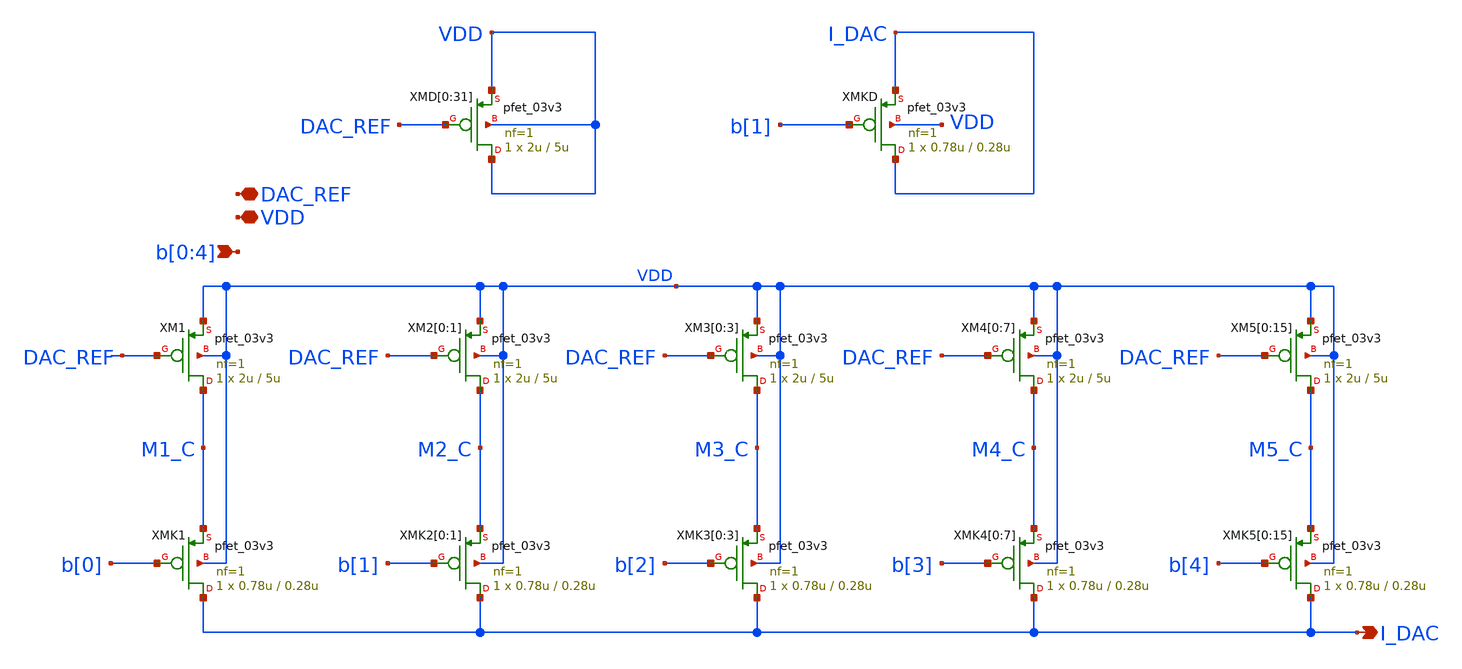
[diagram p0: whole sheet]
** sch_path: DAC_CORE_5bit/DAC_CORE_5bit.sch
**.subckt DAC_CORE_5bit I_DAC VDD DAC_REF b[0],b[1],b[2],b[3],b[4]
*.opin I_DAC
*.iopin VDD
*.iopin DAC_REF
*.ipin b[0],b[1],b[2],b[3],b[4]
XMK1 I_DAC b[0] M1_C VDD pfet_03v3 L=0.28u W=0.78u nf=1 ad='int((nf+1)/2) * W/nf * 0.18u' as='int((nf+2)/2) * W/nf * 0.18u'
+ pd='2*int((nf+1)/2) * (W/nf + 0.18u)' ps='2*int((nf+2)/2) * (W/nf + 0.18u)' nrd='0.18u / W' nrs='0.18u / W'
+ sa=0 sb=0 sd=0 m=1
XMK2[0] I_DAC b[1] M2_C VDD pfet_03v3 L=0.28u W=0.78u nf=1 ad='int((nf+1)/2) * W/nf * 0.18u' as='int((nf+2)/2) * W/nf * 0.18u'
+ pd='2*int((nf+1)/2) * (W/nf + 0.18u)' ps='2*int((nf+2)/2) * (W/nf + 0.18u)' nrd='0.18u / W' nrs='0.18u / W'
+ sa=0 sb=0 sd=0 m=1
XMK2[1] I_DAC b[1] M2_C VDD pfet_03v3 L=0.28u W=0.78u nf=1 ad='int((nf+1)/2) * W/nf * 0.18u' as='int((nf+2)/2) * W/nf * 0.18u'
+ pd='2*int((nf+1)/2) * (W/nf + 0.18u)' ps='2*int((nf+2)/2) * (W/nf + 0.18u)' nrd='0.18u / W' nrs='0.18u / W'
+ sa=0 sb=0 sd=0 m=1
XMK3[0] I_DAC b[2] M3_C VDD pfet_03v3 L=0.28u W=0.78u nf=1 ad='int((nf+1)/2) * W/nf * 0.18u' as='int((nf+2)/2) * W/nf * 0.18u'
+ pd='2*int((nf+1)/2) * (W/nf + 0.18u)' ps='2*int((nf+2)/2) * (W/nf + 0.18u)' nrd='0.18u / W' nrs='0.18u / W'
+ sa=0 sb=0 sd=0 m=1
XMK3[1] I_DAC b[2] M3_C VDD pfet_03v3 L=0.28u W=0.78u nf=1 ad='int((nf+1)/2) * W/nf * 0.18u' as='int((nf+2)/2) * W/nf * 0.18u'
+ pd='2*int((nf+1)/2) * (W/nf + 0.18u)' ps='2*int((nf+2)/2) * (W/nf + 0.18u)' nrd='0.18u / W' nrs='0.18u / W'
+ sa=0 sb=0 sd=0 m=1
XMK3[2] I_DAC b[2] M3_C VDD pfet_03v3 L=0.28u W=0.78u nf=1 ad='int((nf+1)/2) * W/nf * 0.18u' as='int((nf+2)/2) * W/nf * 0.18u'
+ pd='2*int((nf+1)/2) * (W/nf + 0.18u)' ps='2*int((nf+2)/2) * (W/nf + 0.18u)' nrd='0.18u / W' nrs='0.18u / W'
+ sa=0 sb=0 sd=0 m=1
XMK3[3] I_DAC b[2] M3_C VDD pfet_03v3 L=0.28u W=0.78u nf=1 ad='int((nf+1)/2) * W/nf * 0.18u' as='int((nf+2)/2) * W/nf * 0.18u'
+ pd='2*int((nf+1)/2) * (W/nf + 0.18u)' ps='2*int((nf+2)/2) * (W/nf + 0.18u)' nrd='0.18u / W' nrs='0.18u / W'
+ sa=0 sb=0 sd=0 m=1
XMK4[0] I_DAC b[3] M4_C VDD pfet_03v3 L=0.28u W=0.78u nf=1 ad='int((nf+1)/2) * W/nf * 0.18u' as='int((nf+2)/2) * W/nf * 0.18u'
+ pd='2*int((nf+1)/2) * (W/nf + 0.18u)' ps='2*int((nf+2)/2) * (W/nf + 0.18u)' nrd='0.18u / W' nrs='0.18u / W'
+ sa=0 sb=0 sd=0 m=1
XMK4[1] I_DAC b[3] M4_C VDD pfet_03v3 L=0.28u W=0.78u nf=1 ad='int((nf+1)/2) * W/nf * 0.18u' as='int((nf+2)/2) * W/nf * 0.18u'
+ pd='2*int((nf+1)/2) * (W/nf + 0.18u)' ps='2*int((nf+2)/2) * (W/nf + 0.18u)' nrd='0.18u / W' nrs='0.18u / W'
+ sa=0 sb=0 sd=0 m=1
XMK4[2] I_DAC b[3] M4_C VDD pfet_03v3 L=0.28u W=0.78u nf=1 ad='int((nf+1)/2) * W/nf * 0.18u' as='int((nf+2)/2) * W/nf * 0.18u'
+ pd='2*int((nf+1)/2) * (W/nf + 0.18u)' ps='2*int((nf+2)/2) * (W/nf + 0.18u)' nrd='0.18u / W' nrs='0.18u / W'
+ sa=0 sb=0 sd=0 m=1
XMK4[3] I_DAC b[3] M4_C VDD pfet_03v3 L=0.28u W=0.78u nf=1 ad='int((nf+1)/2) * W/nf * 0.18u' as='int((nf+2)/2) * W/nf * 0.18u'
+ pd='2*int((nf+1)/2) * (W/nf + 0.18u)' ps='2*int((nf+2)/2) * (W/nf + 0.18u)' nrd='0.18u / W' nrs='0.18u / W'
+ sa=0 sb=0 sd=0 m=1
XMK4[4] I_DAC b[3] M4_C VDD pfet_03v3 L=0.28u W=0.78u nf=1 ad='int((nf+1)/2) * W/nf * 0.18u' as='int((nf+2)/2) * W/nf * 0.18u'
+ pd='2*int((nf+1)/2) * (W/nf + 0.18u)' ps='2*int((nf+2)/2) * (W/nf + 0.18u)' nrd='0.18u / W' nrs='0.18u / W'
+ sa=0 sb=0 sd=0 m=1
XMK4[5] I_DAC b[3] M4_C VDD pfet_03v3 L=0.28u W=0.78u nf=1 ad='int((nf+1)/2) * W/nf * 0.18u' as='int((nf+2)/2) * W/nf * 0.18u'
+ pd='2*int((nf+1)/2) * (W/nf + 0.18u)' ps='2*int((nf+2)/2) * (W/nf + 0.18u)' nrd='0.18u / W' nrs='0.18u / W'
+ sa=0 sb=0 sd=0 m=1
XMK4[6] I_DAC b[3] M4_C VDD pfet_03v3 L=0.28u W=0.78u nf=1 ad='int((nf+1)/2) * W/nf * 0.18u' as='int((nf+2)/2) * W/nf * 0.18u'
+ pd='2*int((nf+1)/2) * (W/nf + 0.18u)' ps='2*int((nf+2)/2) * (W/nf + 0.18u)' nrd='0.18u / W' nrs='0.18u / W'
+ sa=0 sb=0 sd=0 m=1
XMK4[7] I_DAC b[3] M4_C VDD pfet_03v3 L=0.28u W=0.78u nf=1 ad='int((nf+1)/2) * W/nf * 0.18u' as='int((nf+2)/2) * W/nf * 0.18u'
+ pd='2*int((nf+1)/2) * (W/nf + 0.18u)' ps='2*int((nf+2)/2) * (W/nf + 0.18u)' nrd='0.18u / W' nrs='0.18u / W'
+ sa=0 sb=0 sd=0 m=1
XMK5[0] I_DAC b[4] M5_C VDD pfet_03v3 L=0.28u W=0.78u nf=1 ad='int((nf+1)/2) * W/nf * 0.18u' as='int((nf+2)/2) * W/nf * 0.18u'
+ pd='2*int((nf+1)/2) * (W/nf + 0.18u)' ps='2*int((nf+2)/2) * (W/nf + 0.18u)' nrd='0.18u / W' nrs='0.18u / W'
+ sa=0 sb=0 sd=0 m=1
XMK5[1] I_DAC b[4] M5_C VDD pfet_03v3 L=0.28u W=0.78u nf=1 ad='int((nf+1)/2) * W/nf * 0.18u' as='int((nf+2)/2) * W/nf * 0.18u'
+ pd='2*int((nf+1)/2) * (W/nf + 0.18u)' ps='2*int((nf+2)/2) * (W/nf + 0.18u)' nrd='0.18u / W' nrs='0.18u / W'
+ sa=0 sb=0 sd=0 m=1
XMK5[2] I_DAC b[4] M5_C VDD pfet_03v3 L=0.28u W=0.78u nf=1 ad='int((nf+1)/2) * W/nf * 0.18u' as='int((nf+2)/2) * W/nf * 0.18u'
+ pd='2*int((nf+1)/2) * (W/nf + 0.18u)' ps='2*int((nf+2)/2) * (W/nf + 0.18u)' nrd='0.18u / W' nrs='0.18u / W'
+ sa=0 sb=0 sd=0 m=1
XMK5[3] I_DAC b[4] M5_C VDD pfet_03v3 L=0.28u W=0.78u nf=1 ad='int((nf+1)/2) * W/nf * 0.18u' as='int((nf+2)/2) * W/nf * 0.18u'
+ pd='2*int((nf+1)/2) * (W/nf + 0.18u)' ps='2*int((nf+2)/2) * (W/nf + 0.18u)' nrd='0.18u / W' nrs='0.18u / W'
+ sa=0 sb=0 sd=0 m=1
XMK5[4] I_DAC b[4] M5_C VDD pfet_03v3 L=0.28u W=0.78u nf=1 ad='int((nf+1)/2) * W/nf * 0.18u' as='int((nf+2)/2) * W/nf * 0.18u'
+ pd='2*int((nf+1)/2) * (W/nf + 0.18u)' ps='2*int((nf+2)/2) * (W/nf + 0.18u)' nrd='0.18u / W' nrs='0.18u / W'
+ sa=0 sb=0 sd=0 m=1
XMK5[5] I_DAC b[4] M5_C VDD pfet_03v3 L=0.28u W=0.78u nf=1 ad='int((nf+1)/2) * W/nf * 0.18u' as='int((nf+2)/2) * W/nf * 0.18u'
+ pd='2*int((nf+1)/2) * (W/nf + 0.18u)' ps='2*int((nf+2)/2) * (W/nf + 0.18u)' nrd='0.18u / W' nrs='0.18u / W'
+ sa=0 sb=0 sd=0 m=1
XMK5[6] I_DAC b[4] M5_C VDD pfet_03v3 L=0.28u W=0.78u nf=1 ad='int((nf+1)/2) * W/nf * 0.18u' as='int((nf+2)/2) * W/nf * 0.18u'
+ pd='2*int((nf+1)/2) * (W/nf + 0.18u)' ps='2*int((nf+2)/2) * (W/nf + 0.18u)' nrd='0.18u / W' nrs='0.18u / W'
+ sa=0 sb=0 sd=0 m=1
XMK5[7] I_DAC b[4] M5_C VDD pfet_03v3 L=0.28u W=0.78u nf=1 ad='int((nf+1)/2) * W/nf * 0.18u' as='int((nf+2)/2) * W/nf * 0.18u'
+ pd='2*int((nf+1)/2) * (W/nf + 0.18u)' ps='2*int((nf+2)/2) * (W/nf + 0.18u)' nrd='0.18u / W' nrs='0.18u / W'
+ sa=0 sb=0 sd=0 m=1
XMK5[8] I_DAC b[4] M5_C VDD pfet_03v3 L=0.28u W=0.78u nf=1 ad='int((nf+1)/2) * W/nf * 0.18u' as='int((nf+2)/2) * W/nf * 0.18u'
+ pd='2*int((nf+1)/2) * (W/nf + 0.18u)' ps='2*int((nf+2)/2) * (W/nf + 0.18u)' nrd='0.18u / W' nrs='0.18u / W'
+ sa=0 sb=0 sd=0 m=1
XMK5[9] I_DAC b[4] M5_C VDD pfet_03v3 L=0.28u W=0.78u nf=1 ad='int((nf+1)/2) * W/nf * 0.18u' as='int((nf+2)/2) * W/nf * 0.18u'
+ pd='2*int((nf+1)/2) * (W/nf + 0.18u)' ps='2*int((nf+2)/2) * (W/nf + 0.18u)' nrd='0.18u / W' nrs='0.18u / W'
+ sa=0 sb=0 sd=0 m=1
XMK5[10] I_DAC b[4] M5_C VDD pfet_03v3 L=0.28u W=0.78u nf=1 ad='int((nf+1)/2) * W/nf * 0.18u' as='int((nf+2)/2) * W/nf * 0.18u'
+ pd='2*int((nf+1)/2) * (W/nf + 0.18u)' ps='2*int((nf+2)/2) * (W/nf + 0.18u)' nrd='0.18u / W' nrs='0.18u / W'
+ sa=0 sb=0 sd=0 m=1
XMK5[11] I_DAC b[4] M5_C VDD pfet_03v3 L=0.28u W=0.78u nf=1 ad='int((nf+1)/2) * W/nf * 0.18u' as='int((nf+2)/2) * W/nf * 0.18u'
+ pd='2*int((nf+1)/2) * (W/nf + 0.18u)' ps='2*int((nf+2)/2) * (W/nf + 0.18u)' nrd='0.18u / W' nrs='0.18u / W'
+ sa=0 sb=0 sd=0 m=1
XMK5[12] I_DAC b[4] M5_C VDD pfet_03v3 L=0.28u W=0.78u nf=1 ad='int((nf+1)/2) * W/nf * 0.18u' as='int((nf+2)/2) * W/nf * 0.18u'
+ pd='2*int((nf+1)/2) * (W/nf + 0.18u)' ps='2*int((nf+2)/2) * (W/nf + 0.18u)' nrd='0.18u / W' nrs='0.18u / W'
+ sa=0 sb=0 sd=0 m=1
XMK5[13] I_DAC b[4] M5_C VDD pfet_03v3 L=0.28u W=0.78u nf=1 ad='int((nf+1)/2) * W/nf * 0.18u' as='int((nf+2)/2) * W/nf * 0.18u'
+ pd='2*int((nf+1)/2) * (W/nf + 0.18u)' ps='2*int((nf+2)/2) * (W/nf + 0.18u)' nrd='0.18u / W' nrs='0.18u / W'
+ sa=0 sb=0 sd=0 m=1
XMK5[14] I_DAC b[4] M5_C VDD pfet_03v3 L=0.28u W=0.78u nf=1 ad='int((nf+1)/2) * W/nf * 0.18u' as='int((nf+2)/2) * W/nf * 0.18u'
+ pd='2*int((nf+1)/2) * (W/nf + 0.18u)' ps='2*int((nf+2)/2) * (W/nf + 0.18u)' nrd='0.18u / W' nrs='0.18u / W'
+ sa=0 sb=0 sd=0 m=1
XMK5[15] I_DAC b[4] M5_C VDD pfet_03v3 L=0.28u W=0.78u nf=1 ad='int((nf+1)/2) * W/nf * 0.18u' as='int((nf+2)/2) * W/nf * 0.18u'
+ pd='2*int((nf+1)/2) * (W/nf + 0.18u)' ps='2*int((nf+2)/2) * (W/nf + 0.18u)' nrd='0.18u / W' nrs='0.18u / W'
+ sa=0 sb=0 sd=0 m=1
XM1 M1_C DAC_REF VDD VDD pfet_03v3 L=5u W=2u nf=1 ad='int((nf+1)/2) * W/nf * 0.18u' as='int((nf+2)/2) * W/nf * 0.18u'
+ pd='2*int((nf+1)/2) * (W/nf + 0.18u)' ps='2*int((nf+2)/2) * (W/nf + 0.18u)' nrd='0.18u / W' nrs='0.18u / W'
+ sa=0 sb=0 sd=0 m=1
XM2[0] M2_C DAC_REF VDD VDD pfet_03v3 L=5u W=2u nf=1 ad='int((nf+1)/2) * W/nf * 0.18u' as='int((nf+2)/2) * W/nf * 0.18u'
+ pd='2*int((nf+1)/2) * (W/nf + 0.18u)' ps='2*int((nf+2)/2) * (W/nf + 0.18u)' nrd='0.18u / W' nrs='0.18u / W'
+ sa=0 sb=0 sd=0 m=1
XM2[1] M2_C DAC_REF VDD VDD pfet_03v3 L=5u W=2u nf=1 ad='int((nf+1)/2) * W/nf * 0.18u' as='int((nf+2)/2) * W/nf * 0.18u'
+ pd='2*int((nf+1)/2) * (W/nf + 0.18u)' ps='2*int((nf+2)/2) * (W/nf + 0.18u)' nrd='0.18u / W' nrs='0.18u / W'
+ sa=0 sb=0 sd=0 m=1
XM3[0] M3_C DAC_REF VDD VDD pfet_03v3 L=5u W=2u nf=1 ad='int((nf+1)/2) * W/nf * 0.18u' as='int((nf+2)/2) * W/nf * 0.18u'
+ pd='2*int((nf+1)/2) * (W/nf + 0.18u)' ps='2*int((nf+2)/2) * (W/nf + 0.18u)' nrd='0.18u / W' nrs='0.18u / W'
+ sa=0 sb=0 sd=0 m=1
XM3[1] M3_C DAC_REF VDD VDD pfet_03v3 L=5u W=2u nf=1 ad='int((nf+1)/2) * W/nf * 0.18u' as='int((nf+2)/2) * W/nf * 0.18u'
+ pd='2*int((nf+1)/2) * (W/nf + 0.18u)' ps='2*int((nf+2)/2) * (W/nf + 0.18u)' nrd='0.18u / W' nrs='0.18u / W'
+ sa=0 sb=0 sd=0 m=1
XM3[2] M3_C DAC_REF VDD VDD pfet_03v3 L=5u W=2u nf=1 ad='int((nf+1)/2) * W/nf * 0.18u' as='int((nf+2)/2) * W/nf * 0.18u'
+ pd='2*int((nf+1)/2) * (W/nf + 0.18u)' ps='2*int((nf+2)/2) * (W/nf + 0.18u)' nrd='0.18u / W' nrs='0.18u / W'
+ sa=0 sb=0 sd=0 m=1
XM3[3] M3_C DAC_REF VDD VDD pfet_03v3 L=5u W=2u nf=1 ad='int((nf+1)/2) * W/nf * 0.18u' as='int((nf+2)/2) * W/nf * 0.18u'
+ pd='2*int((nf+1)/2) * (W/nf + 0.18u)' ps='2*int((nf+2)/2) * (W/nf + 0.18u)' nrd='0.18u / W' nrs='0.18u / W'
+ sa=0 sb=0 sd=0 m=1
XM4[0] M4_C DAC_REF VDD VDD pfet_03v3 L=5u W=2u nf=1 ad='int((nf+1)/2) * W/nf * 0.18u' as='int((nf+2)/2) * W/nf * 0.18u'
+ pd='2*int((nf+1)/2) * (W/nf + 0.18u)' ps='2*int((nf+2)/2) * (W/nf + 0.18u)' nrd='0.18u / W' nrs='0.18u / W'
+ sa=0 sb=0 sd=0 m=1
XM4[1] M4_C DAC_REF VDD VDD pfet_03v3 L=5u W=2u nf=1 ad='int((nf+1)/2) * W/nf * 0.18u' as='int((nf+2)/2) * W/nf * 0.18u'
+ pd='2*int((nf+1)/2) * (W/nf + 0.18u)' ps='2*int((nf+2)/2) * (W/nf + 0.18u)' nrd='0.18u / W' nrs='0.18u / W'
+ sa=0 sb=0 sd=0 m=1
XM4[2] M4_C DAC_REF VDD VDD pfet_03v3 L=5u W=2u nf=1 ad='int((nf+1)/2) * W/nf * 0.18u' as='int((nf+2)/2) * W/nf * 0.18u'
+ pd='2*int((nf+1)/2) * (W/nf + 0.18u)' ps='2*int((nf+2)/2) * (W/nf + 0.18u)' nrd='0.18u / W' nrs='0.18u / W'
+ sa=0 sb=0 sd=0 m=1
XM4[3] M4_C DAC_REF VDD VDD pfet_03v3 L=5u W=2u nf=1 ad='int((nf+1)/2) * W/nf * 0.18u' as='int((nf+2)/2) * W/nf * 0.18u'
+ pd='2*int((nf+1)/2) * (W/nf + 0.18u)' ps='2*int((nf+2)/2) * (W/nf + 0.18u)' nrd='0.18u / W' nrs='0.18u / W'
+ sa=0 sb=0 sd=0 m=1
XM4[4] M4_C DAC_REF VDD VDD pfet_03v3 L=5u W=2u nf=1 ad='int((nf+1)/2) * W/nf * 0.18u' as='int((nf+2)/2) * W/nf * 0.18u'
+ pd='2*int((nf+1)/2) * (W/nf + 0.18u)' ps='2*int((nf+2)/2) * (W/nf + 0.18u)' nrd='0.18u / W' nrs='0.18u / W'
+ sa=0 sb=0 sd=0 m=1
XM4[5] M4_C DAC_REF VDD VDD pfet_03v3 L=5u W=2u nf=1 ad='int((nf+1)/2) * W/nf * 0.18u' as='int((nf+2)/2) * W/nf * 0.18u'
+ pd='2*int((nf+1)/2) * (W/nf + 0.18u)' ps='2*int((nf+2)/2) * (W/nf + 0.18u)' nrd='0.18u / W' nrs='0.18u / W'
+ sa=0 sb=0 sd=0 m=1
XM4[6] M4_C DAC_REF VDD VDD pfet_03v3 L=5u W=2u nf=1 ad='int((nf+1)/2) * W/nf * 0.18u' as='int((nf+2)/2) * W/nf * 0.18u'
+ pd='2*int((nf+1)/2) * (W/nf + 0.18u)' ps='2*int((nf+2)/2) * (W/nf + 0.18u)' nrd='0.18u / W' nrs='0.18u / W'
+ sa=0 sb=0 sd=0 m=1
XM4[7] M4_C DAC_REF VDD VDD pfet_03v3 L=5u W=2u nf=1 ad='int((nf+1)/2) * W/nf * 0.18u' as='int((nf+2)/2) * W/nf * 0.18u'
+ pd='2*int((nf+1)/2) * (W/nf + 0.18u)' ps='2*int((nf+2)/2) * (W/nf + 0.18u)' nrd='0.18u / W' nrs='0.18u / W'
+ sa=0 sb=0 sd=0 m=1
XM5[0] M5_C DAC_REF VDD VDD pfet_03v3 L=5u W=2u nf=1 ad='int((nf+1)/2) * W/nf * 0.18u' as='int((nf+2)/2) * W/nf * 0.18u'
+ pd='2*int((nf+1)/2) * (W/nf + 0.18u)' ps='2*int((nf+2)/2) * (W/nf + 0.18u)' nrd='0.18u / W' nrs='0.18u / W'
+ sa=0 sb=0 sd=0 m=1
XM5[1] M5_C DAC_REF VDD VDD pfet_03v3 L=5u W=2u nf=1 ad='int((nf+1)/2) * W/nf * 0.18u' as='int((nf+2)/2) * W/nf * 0.18u'
+ pd='2*int((nf+1)/2) * (W/nf + 0.18u)' ps='2*int((nf+2)/2) * (W/nf + 0.18u)' nrd='0.18u / W' nrs='0.18u / W'
+ sa=0 sb=0 sd=0 m=1
XM5[2] M5_C DAC_REF VDD VDD pfet_03v3 L=5u W=2u nf=1 ad='int((nf+1)/2) * W/nf * 0.18u' as='int((nf+2)/2) * W/nf * 0.18u'
+ pd='2*int((nf+1)/2) * (W/nf + 0.18u)' ps='2*int((nf+2)/2) * (W/nf + 0.18u)' nrd='0.18u / W' nrs='0.18u / W'
+ sa=0 sb=0 sd=0 m=1
XM5[3] M5_C DAC_REF VDD VDD pfet_03v3 L=5u W=2u nf=1 ad='int((nf+1)/2) * W/nf * 0.18u' as='int((nf+2)/2) * W/nf * 0.18u'
+ pd='2*int((nf+1)/2) * (W/nf + 0.18u)' ps='2*int((nf+2)/2) * (W/nf + 0.18u)' nrd='0.18u / W' nrs='0.18u / W'
+ sa=0 sb=0 sd=0 m=1
XM5[4] M5_C DAC_REF VDD VDD pfet_03v3 L=5u W=2u nf=1 ad='int((nf+1)/2) * W/nf * 0.18u' as='int((nf+2)/2) * W/nf * 0.18u'
+ pd='2*int((nf+1)/2) * (W/nf + 0.18u)' ps='2*int((nf+2)/2) * (W/nf + 0.18u)' nrd='0.18u / W' nrs='0.18u / W'
+ sa=0 sb=0 sd=0 m=1
XM5[5] M5_C DAC_REF VDD VDD pfet_03v3 L=5u W=2u nf=1 ad='int((nf+1)/2) * W/nf * 0.18u' as='int((nf+2)/2) * W/nf * 0.18u'
+ pd='2*int((nf+1)/2) * (W/nf + 0.18u)' ps='2*int((nf+2)/2) * (W/nf + 0.18u)' nrd='0.18u / W' nrs='0.18u / W'
+ sa=0 sb=0 sd=0 m=1
XM5[6] M5_C DAC_REF VDD VDD pfet_03v3 L=5u W=2u nf=1 ad='int((nf+1)/2) * W/nf * 0.18u' as='int((nf+2)/2) * W/nf * 0.18u'
+ pd='2*int((nf+1)/2) * (W/nf + 0.18u)' ps='2*int((nf+2)/2) * (W/nf + 0.18u)' nrd='0.18u / W' nrs='0.18u / W'
+ sa=0 sb=0 sd=0 m=1
XM5[7] M5_C DAC_REF VDD VDD pfet_03v3 L=5u W=2u nf=1 ad='int((nf+1)/2) * W/nf * 0.18u' as='int((nf+2)/2) * W/nf * 0.18u'
+ pd='2*int((nf+1)/2) * (W/nf + 0.18u)' ps='2*int((nf+2)/2) * (W/nf + 0.18u)' nrd='0.18u / W' nrs='0.18u / W'
+ sa=0 sb=0 sd=0 m=1
XM5[8] M5_C DAC_REF VDD VDD pfet_03v3 L=5u W=2u nf=1 ad='int((nf+1)/2) * W/nf * 0.18u' as='int((nf+2)/2) * W/nf * 0.18u'
+ pd='2*int((nf+1)/2) * (W/nf + 0.18u)' ps='2*int((nf+2)/2) * (W/nf + 0.18u)' nrd='0.18u / W' nrs='0.18u / W'
+ sa=0 sb=0 sd=0 m=1
XM5[9] M5_C DAC_REF VDD VDD pfet_03v3 L=5u W=2u nf=1 ad='int((nf+1)/2) * W/nf * 0.18u' as='int((nf+2)/2) * W/nf * 0.18u'
+ pd='2*int((nf+1)/2) * (W/nf + 0.18u)' ps='2*int((nf+2)/2) * (W/nf + 0.18u)' nrd='0.18u / W' nrs='0.18u / W'
+ sa=0 sb=0 sd=0 m=1
XM5[10] M5_C DAC_REF VDD VDD pfet_03v3 L=5u W=2u nf=1 ad='int((nf+1)/2) * W/nf * 0.18u' as='int((nf+2)/2) * W/nf * 0.18u'
+ pd='2*int((nf+1)/2) * (W/nf + 0.18u)' ps='2*int((nf+2)/2) * (W/nf + 0.18u)' nrd='0.18u / W' nrs='0.18u / W'
+ sa=0 sb=0 sd=0 m=1
XM5[11] M5_C DAC_REF VDD VDD pfet_03v3 L=5u W=2u nf=1 ad='int((nf+1)/2) * W/nf * 0.18u' as='int((nf+2)/2) * W/nf * 0.18u'
+ pd='2*int((nf+1)/2) * (W/nf + 0.18u)' ps='2*int((nf+2)/2) * (W/nf + 0.18u)' nrd='0.18u / W' nrs='0.18u / W'
+ sa=0 sb=0 sd=0 m=1
XM5[12] M5_C DAC_REF VDD VDD pfet_03v3 L=5u W=2u nf=1 ad='int((nf+1)/2) * W/nf * 0.18u' as='int((nf+2)/2) * W/nf * 0.18u'
+ pd='2*int((nf+1)/2) * (W/nf + 0.18u)' ps='2*int((nf+2)/2) * (W/nf + 0.18u)' nrd='0.18u / W' nrs='0.18u / W'
+ sa=0 sb=0 sd=0 m=1
XM5[13] M5_C DAC_REF VDD VDD pfet_03v3 L=5u W=2u nf=1 ad='int((nf+1)/2) * W/nf * 0.18u' as='int((nf+2)/2) * W/nf * 0.18u'
+ pd='2*int((nf+1)/2) * (W/nf + 0.18u)' ps='2*int((nf+2)/2) * (W/nf + 0.18u)' nrd='0.18u / W' nrs='0.18u / W'
+ sa=0 sb=0 sd=0 m=1
XM5[14] M5_C DAC_REF VDD VDD pfet_03v3 L=5u W=2u nf=1 ad='int((nf+1)/2) * W/nf * 0.18u' as='int((nf+2)/2) * W/nf * 0.18u'
+ pd='2*int((nf+1)/2) * (W/nf + 0.18u)' ps='2*int((nf+2)/2) * (W/nf + 0.18u)' nrd='0.18u / W' nrs='0.18u / W'
+ sa=0 sb=0 sd=0 m=1
XM5[15] M5_C DAC_REF VDD VDD pfet_03v3 L=5u W=2u nf=1 ad='int((nf+1)/2) * W/nf * 0.18u' as='int((nf+2)/2) * W/nf * 0.18u'
+ pd='2*int((nf+1)/2) * (W/nf + 0.18u)' ps='2*int((nf+2)/2) * (W/nf + 0.18u)' nrd='0.18u / W' nrs='0.18u / W'
+ sa=0 sb=0 sd=0 m=1
XMD[0] VDD DAC_REF VDD VDD pfet_03v3 L=5u W=2u nf=1 ad='int((nf+1)/2) * W/nf * 0.18u' as='int((nf+2)/2) * W/nf * 0.18u'
+ pd='2*int((nf+1)/2) * (W/nf + 0.18u)' ps='2*int((nf+2)/2) * (W/nf + 0.18u)' nrd='0.18u / W' nrs='0.18u / W'
+ sa=0 sb=0 sd=0 m=1
XMD[1] VDD DAC_REF VDD VDD pfet_03v3 L=5u W=2u nf=1 ad='int((nf+1)/2) * W/nf * 0.18u' as='int((nf+2)/2) * W/nf * 0.18u'
+ pd='2*int((nf+1)/2) * (W/nf + 0.18u)' ps='2*int((nf+2)/2) * (W/nf + 0.18u)' nrd='0.18u / W' nrs='0.18u / W'
+ sa=0 sb=0 sd=0 m=1
XMD[2] VDD DAC_REF VDD VDD pfet_03v3 L=5u W=2u nf=1 ad='int((nf+1)/2) * W/nf * 0.18u' as='int((nf+2)/2) * W/nf * 0.18u'
+ pd='2*int((nf+1)/2) * (W/nf + 0.18u)' ps='2*int((nf+2)/2) * (W/nf + 0.18u)' nrd='0.18u / W' nrs='0.18u / W'
+ sa=0 sb=0 sd=0 m=1
XMD[3] VDD DAC_REF VDD VDD pfet_03v3 L=5u W=2u nf=1 ad='int((nf+1)/2) * W/nf * 0.18u' as='int((nf+2)/2) * W/nf * 0.18u'
+ pd='2*int((nf+1)/2) * (W/nf + 0.18u)' ps='2*int((nf+2)/2) * (W/nf + 0.18u)' nrd='0.18u / W' nrs='0.18u / W'
+ sa=0 sb=0 sd=0 m=1
XMD[4] VDD DAC_REF VDD VDD pfet_03v3 L=5u W=2u nf=1 ad='int((nf+1)/2) * W/nf * 0.18u' as='int((nf+2)/2) * W/nf * 0.18u'
+ pd='2*int((nf+1)/2) * (W/nf + 0.18u)' ps='2*int((nf+2)/2) * (W/nf + 0.18u)' nrd='0.18u / W' nrs='0.18u / W'
+ sa=0 sb=0 sd=0 m=1
XMD[5] VDD DAC_REF VDD VDD pfet_03v3 L=5u W=2u nf=1 ad='int((nf+1)/2) * W/nf * 0.18u' as='int((nf+2)/2) * W/nf * 0.18u'
+ pd='2*int((nf+1)/2) * (W/nf + 0.18u)' ps='2*int((nf+2)/2) * (W/nf + 0.18u)' nrd='0.18u / W' nrs='0.18u / W'
+ sa=0 sb=0 sd=0 m=1
XMD[6] VDD DAC_REF VDD VDD pfet_03v3 L=5u W=2u nf=1 ad='int((nf+1)/2) * W/nf * 0.18u' as='int((nf+2)/2) * W/nf * 0.18u'
+ pd='2*int((nf+1)/2) * (W/nf + 0.18u)' ps='2*int((nf+2)/2) * (W/nf + 0.18u)' nrd='0.18u / W' nrs='0.18u / W'
+ sa=0 sb=0 sd=0 m=1
XMD[7] VDD DAC_REF VDD VDD pfet_03v3 L=5u W=2u nf=1 ad='int((nf+1)/2) * W/nf * 0.18u' as='int((nf+2)/2) * W/nf * 0.18u'
+ pd='2*int((nf+1)/2) * (W/nf + 0.18u)' ps='2*int((nf+2)/2) * (W/nf + 0.18u)' nrd='0.18u / W' nrs='0.18u / W'
+ sa=0 sb=0 sd=0 m=1
XMD[8] VDD DAC_REF VDD VDD pfet_03v3 L=5u W=2u nf=1 ad='int((nf+1)/2) * W/nf * 0.18u' as='int((nf+2)/2) * W/nf * 0.18u'
+ pd='2*int((nf+1)/2) * (W/nf + 0.18u)' ps='2*int((nf+2)/2) * (W/nf + 0.18u)' nrd='0.18u / W' nrs='0.18u / W'
+ sa=0 sb=0 sd=0 m=1
XMD[9] VDD DAC_REF VDD VDD pfet_03v3 L=5u W=2u nf=1 ad='int((nf+1)/2) * W/nf * 0.18u' as='int((nf+2)/2) * W/nf * 0.18u'
+ pd='2*int((nf+1)/2) * (W/nf + 0.18u)' ps='2*int((nf+2)/2) * (W/nf + 0.18u)' nrd='0.18u / W' nrs='0.18u / W'
+ sa=0 sb=0 sd=0 m=1
XMD[10] VDD DAC_REF VDD VDD pfet_03v3 L=5u W=2u nf=1 ad='int((nf+1)/2) * W/nf * 0.18u' as='int((nf+2)/2) * W/nf * 0.18u'
+ pd='2*int((nf+1)/2) * (W/nf + 0.18u)' ps='2*int((nf+2)/2) * (W/nf + 0.18u)' nrd='0.18u / W' nrs='0.18u / W'
+ sa=0 sb=0 sd=0 m=1
XMD[11] VDD DAC_REF VDD VDD pfet_03v3 L=5u W=2u nf=1 ad='int((nf+1)/2) * W/nf * 0.18u' as='int((nf+2)/2) * W/nf * 0.18u'
+ pd='2*int((nf+1)/2) * (W/nf + 0.18u)' ps='2*int((nf+2)/2) * (W/nf + 0.18u)' nrd='0.18u / W' nrs='0.18u / W'
+ sa=0 sb=0 sd=0 m=1
XMD[12] VDD DAC_REF VDD VDD pfet_03v3 L=5u W=2u nf=1 ad='int((nf+1)/2) * W/nf * 0.18u' as='int((nf+2)/2) * W/nf * 0.18u'
+ pd='2*int((nf+1)/2) * (W/nf + 0.18u)' ps='2*int((nf+2)/2) * (W/nf + 0.18u)' nrd='0.18u / W' nrs='0.18u / W'
+ sa=0 sb=0 sd=0 m=1
XMD[13] VDD DAC_REF VDD VDD pfet_03v3 L=5u W=2u nf=1 ad='int((nf+1)/2) * W/nf * 0.18u' as='int((nf+2)/2) * W/nf * 0.18u'
+ pd='2*int((nf+1)/2) * (W/nf + 0.18u)' ps='2*int((nf+2)/2) * (W/nf + 0.18u)' nrd='0.18u / W' nrs='0.18u / W'
+ sa=0 sb=0 sd=0 m=1
XMD[14] VDD DAC_REF VDD VDD pfet_03v3 L=5u W=2u nf=1 ad='int((nf+1)/2) * W/nf * 0.18u' as='int((nf+2)/2) * W/nf * 0.18u'
+ pd='2*int((nf+1)/2) * (W/nf + 0.18u)' ps='2*int((nf+2)/2) * (W/nf + 0.18u)' nrd='0.18u / W' nrs='0.18u / W'
+ sa=0 sb=0 sd=0 m=1
XMD[15] VDD DAC_REF VDD VDD pfet_03v3 L=5u W=2u nf=1 ad='int((nf+1)/2) * W/nf * 0.18u' as='int((nf+2)/2) * W/nf * 0.18u'
+ pd='2*int((nf+1)/2) * (W/nf + 0.18u)' ps='2*int((nf+2)/2) * (W/nf + 0.18u)' nrd='0.18u / W' nrs='0.18u / W'
+ sa=0 sb=0 sd=0 m=1
XMD[16] VDD DAC_REF VDD VDD pfet_03v3 L=5u W=2u nf=1 ad='int((nf+1)/2) * W/nf * 0.18u' as='int((nf+2)/2) * W/nf * 0.18u'
+ pd='2*int((nf+1)/2) * (W/nf + 0.18u)' ps='2*int((nf+2)/2) * (W/nf + 0.18u)' nrd='0.18u / W' nrs='0.18u / W'
+ sa=0 sb=0 sd=0 m=1
XMD[17] VDD DAC_REF VDD VDD pfet_03v3 L=5u W=2u nf=1 ad='int((nf+1)/2) * W/nf * 0.18u' as='int((nf+2)/2) * W/nf * 0.18u'
+ pd='2*int((nf+1)/2) * (W/nf + 0.18u)' ps='2*int((nf+2)/2) * (W/nf + 0.18u)' nrd='0.18u / W' nrs='0.18u / W'
+ sa=0 sb=0 sd=0 m=1
XMD[18] VDD DAC_REF VDD VDD pfet_03v3 L=5u W=2u nf=1 ad='int((nf+1)/2) * W/nf * 0.18u' as='int((nf+2)/2) * W/nf * 0.18u'
+ pd='2*int((nf+1)/2) * (W/nf + 0.18u)' ps='2*int((nf+2)/2) * (W/nf + 0.18u)' nrd='0.18u / W' nrs='0.18u / W'
+ sa=0 sb=0 sd=0 m=1
XMD[19] VDD DAC_REF VDD VDD pfet_03v3 L=5u W=2u nf=1 ad='int((nf+1)/2) * W/nf * 0.18u' as='int((nf+2)/2) * W/nf * 0.18u'
+ pd='2*int((nf+1)/2) * (W/nf + 0.18u)' ps='2*int((nf+2)/2) * (W/nf + 0.18u)' nrd='0.18u / W' nrs='0.18u / W'
+ sa=0 sb=0 sd=0 m=1
XMD[20] VDD DAC_REF VDD VDD pfet_03v3 L=5u W=2u nf=1 ad='int((nf+1)/2) * W/nf * 0.18u' as='int((nf+2)/2) * W/nf * 0.18u'
+ pd='2*int((nf+1)/2) * (W/nf + 0.18u)' ps='2*int((nf+2)/2) * (W/nf + 0.18u)' nrd='0.18u / W' nrs='0.18u / W'
+ sa=0 sb=0 sd=0 m=1
XMD[21] VDD DAC_REF VDD VDD pfet_03v3 L=5u W=2u nf=1 ad='int((nf+1)/2) * W/nf * 0.18u' as='int((nf+2)/2) * W/nf * 0.18u'
+ pd='2*int((nf+1)/2) * (W/nf + 0.18u)' ps='2*int((nf+2)/2) * (W/nf + 0.18u)' nrd='0.18u / W' nrs='0.18u / W'
+ sa=0 sb=0 sd=0 m=1
XMD[22] VDD DAC_REF VDD VDD pfet_03v3 L=5u W=2u nf=1 ad='int((nf+1)/2) * W/nf * 0.18u' as='int((nf+2)/2) * W/nf * 0.18u'
+ pd='2*int((nf+1)/2) * (W/nf + 0.18u)' ps='2*int((nf+2)/2) * (W/nf + 0.18u)' nrd='0.18u / W' nrs='0.18u / W'
+ sa=0 sb=0 sd=0 m=1
XMD[23] VDD DAC_REF VDD VDD pfet_03v3 L=5u W=2u nf=1 ad='int((nf+1)/2) * W/nf * 0.18u' as='int((nf+2)/2) * W/nf * 0.18u'
+ pd='2*int((nf+1)/2) * (W/nf + 0.18u)' ps='2*int((nf+2)/2) * (W/nf + 0.18u)' nrd='0.18u / W' nrs='0.18u / W'
+ sa=0 sb=0 sd=0 m=1
XMD[24] VDD DAC_REF VDD VDD pfet_03v3 L=5u W=2u nf=1 ad='int((nf+1)/2) * W/nf * 0.18u' as='int((nf+2)/2) * W/nf * 0.18u'
+ pd='2*int((nf+1)/2) * (W/nf + 0.18u)' ps='2*int((nf+2)/2) * (W/nf + 0.18u)' nrd='0.18u / W' nrs='0.18u / W'
+ sa=0 sb=0 sd=0 m=1
XMD[25] VDD DAC_REF VDD VDD pfet_03v3 L=5u W=2u nf=1 ad='int((nf+1)/2) * W/nf * 0.18u' as='int((nf+2)/2) * W/nf * 0.18u'
+ pd='2*int((nf+1)/2) * (W/nf + 0.18u)' ps='2*int((nf+2)/2) * (W/nf + 0.18u)' nrd='0.18u / W' nrs='0.18u / W'
+ sa=0 sb=0 sd=0 m=1
XMD[26] VDD DAC_REF VDD VDD pfet_03v3 L=5u W=2u nf=1 ad='int((nf+1)/2) * W/nf * 0.18u' as='int((nf+2)/2) * W/nf * 0.18u'
+ pd='2*int((nf+1)/2) * (W/nf + 0.18u)' ps='2*int((nf+2)/2) * (W/nf + 0.18u)' nrd='0.18u / W' nrs='0.18u / W'
+ sa=0 sb=0 sd=0 m=1
XMD[27] VDD DAC_REF VDD VDD pfet_03v3 L=5u W=2u nf=1 ad='int((nf+1)/2) * W/nf * 0.18u' as='int((nf+2)/2) * W/nf * 0.18u'
+ pd='2*int((nf+1)/2) * (W/nf + 0.18u)' ps='2*int((nf+2)/2) * (W/nf + 0.18u)' nrd='0.18u / W' nrs='0.18u / W'
+ sa=0 sb=0 sd=0 m=1
XMD[28] VDD DAC_REF VDD VDD pfet_03v3 L=5u W=2u nf=1 ad='int((nf+1)/2) * W/nf * 0.18u' as='int((nf+2)/2) * W/nf * 0.18u'
+ pd='2*int((nf+1)/2) * (W/nf + 0.18u)' ps='2*int((nf+2)/2) * (W/nf + 0.18u)' nrd='0.18u / W' nrs='0.18u / W'
+ sa=0 sb=0 sd=0 m=1
XMD[29] VDD DAC_REF VDD VDD pfet_03v3 L=5u W=2u nf=1 ad='int((nf+1)/2) * W/nf * 0.18u' as='int((nf+2)/2) * W/nf * 0.18u'
+ pd='2*int((nf+1)/2) * (W/nf + 0.18u)' ps='2*int((nf+2)/2) * (W/nf + 0.18u)' nrd='0.18u / W' nrs='0.18u / W'
+ sa=0 sb=0 sd=0 m=1
XMD[30] VDD DAC_REF VDD VDD pfet_03v3 L=5u W=2u nf=1 ad='int((nf+1)/2) * W/nf * 0.18u' as='int((nf+2)/2) * W/nf * 0.18u'
+ pd='2*int((nf+1)/2) * (W/nf + 0.18u)' ps='2*int((nf+2)/2) * (W/nf + 0.18u)' nrd='0.18u / W' nrs='0.18u / W'
+ sa=0 sb=0 sd=0 m=1
XMD[31] VDD DAC_REF VDD VDD pfet_03v3 L=5u W=2u nf=1 ad='int((nf+1)/2) * W/nf * 0.18u' as='int((nf+2)/2) * W/nf * 0.18u'
+ pd='2*int((nf+1)/2) * (W/nf + 0.18u)' ps='2*int((nf+2)/2) * (W/nf + 0.18u)' nrd='0.18u / W' nrs='0.18u / W'
+ sa=0 sb=0 sd=0 m=1
XMKD I_DAC b[1] I_DAC VDD pfet_03v3 L=0.28u W=0.78u nf=1 ad='int((nf+1)/2) * W/nf * 0.18u' as='int((nf+2)/2) * W/nf * 0.18u'
+ pd='2*int((nf+1)/2) * (W/nf + 0.18u)' ps='2*int((nf+2)/2) * (W/nf + 0.18u)' nrd='0.18u / W' nrs='0.18u / W'
+ sa=0 sb=0 sd=0 m=1
**.ends
.end
